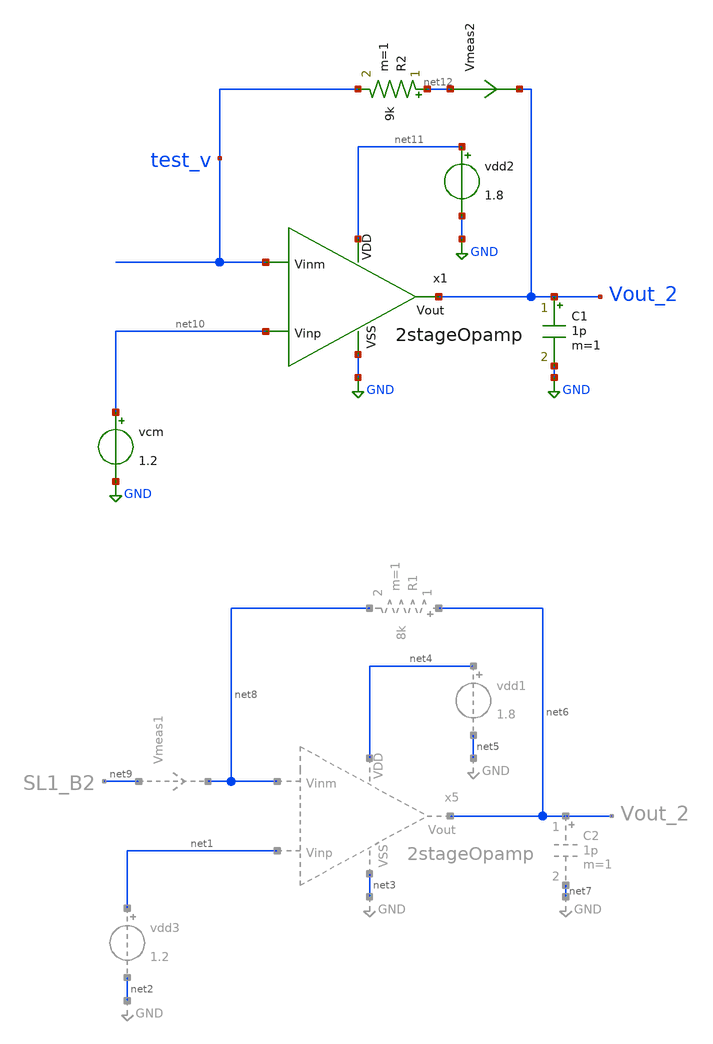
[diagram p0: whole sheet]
** sch_path: xschem/test/xschem/untitled-1.sch
**.subckt untitled-1
x1 net11 test_v net10 Vout_2 GND 2stageOpamp
vdd2 net11 GND 1.8
C1 Vout_2 GND 1p m=1
R2 net12 test_v 9k m=1
Vmeas2 net12 Vout_2 0
.save i(vmeas2)
vcm net10 GND 1.2
**.ends

* expanding   symbol:  amplifiers/dec24/2stageOpamp.sym # of pins=5
** sym_path: amplifiers/dec24/2stageOpamp.sym
** sch_path: amplifiers/dec24/2stageOpamp.sch
.subckt 2stageOpamp VDD Vinm Vinp Vout VSS
*.ipin Vinm
*.ipin Vinp
*.opin Vout
*.ipin VSS
*.ipin VDD
XM8 Vout net1 VSS VSS sky130_fd_pr__nfet_01v8 L=1 W=6 nf=1 ad='int((nf+1)/2) * W/nf * 0.29' as='int((nf+2)/2) * W/nf * 0.29'
+ pd='2*int((nf+1)/2) * (W/nf + 0.29)' ps='2*int((nf+2)/2) * (W/nf + 0.29)' nrd='0.29 / W' nrs='0.29 / W'
+ sa=0 sb=0 sd=0 mult=8 m=8
XM2 Vout Vb1 VDD VDD sky130_fd_pr__pfet_01v8_lvt L=1 W=9 nf=1 ad='int((nf+1)/2) * W/nf * 0.29' as='int((nf+2)/2) * W/nf * 0.29'
+ pd='2*int((nf+1)/2) * (W/nf + 0.29)' ps='2*int((nf+2)/2) * (W/nf + 0.29)' nrd='0.29 / W' nrs='0.29 / W'
+ sa=0 sb=0 sd=0 mult=3 m=3
XM5 net5 Vb3 net6 VSS sky130_fd_pr__nfet_01v8 L=1 W=4 nf=1 ad='int((nf+1)/2) * W/nf * 0.29' as='int((nf+2)/2) * W/nf * 0.29'
+ pd='2*int((nf+1)/2) * (W/nf + 0.29)' ps='2*int((nf+2)/2) * (W/nf + 0.29)' nrd='0.29 / W' nrs='0.29 / W'
+ sa=0 sb=0 sd=0 mult=3 m=3
XM17 net1 Vb3 net7 VSS sky130_fd_pr__nfet_01v8 L=1 W=4 nf=1 ad='int((nf+1)/2) * W/nf * 0.29' as='int((nf+2)/2) * W/nf * 0.29'
+ pd='2*int((nf+1)/2) * (W/nf + 0.29)' ps='2*int((nf+2)/2) * (W/nf + 0.29)' nrd='0.29 / W' nrs='0.29 / W'
+ sa=0 sb=0 sd=0 mult=3 m=3
XM3 net6 net5 VSS VSS sky130_fd_pr__nfet_01v8 L=1 W=8 nf=1 ad='int((nf+1)/2) * W/nf * 0.29' as='int((nf+2)/2) * W/nf * 0.29'
+ pd='2*int((nf+1)/2) * (W/nf + 0.29)' ps='2*int((nf+2)/2) * (W/nf + 0.29)' nrd='0.29 / W' nrs='0.29 / W'
+ sa=0 sb=0 sd=0 mult=1 m=1
XM19 net7 net5 VSS VSS sky130_fd_pr__nfet_01v8 L=1 W=8 nf=1 ad='int((nf+1)/2) * W/nf * 0.29' as='int((nf+2)/2) * W/nf * 0.29'
+ pd='2*int((nf+1)/2) * (W/nf + 0.29)' ps='2*int((nf+2)/2) * (W/nf + 0.29)' nrd='0.29 / W' nrs='0.29 / W'
+ sa=0 sb=0 sd=0 mult=1 m=1
V1 Vb1 GND 1.1
V2 Vb2 GND 0.7
V3 Vb3 GND 0.9
XM11 net8 Vb1 VDD VDD sky130_fd_pr__pfet_01v8_lvt L=1 W=9 nf=1 ad='int((nf+1)/2) * W/nf * 0.29' as='int((nf+2)/2) * W/nf * 0.29'
+ pd='2*int((nf+1)/2) * (W/nf + 0.29)' ps='2*int((nf+2)/2) * (W/nf + 0.29)' nrd='0.29 / W' nrs='0.29 / W'
+ sa=0 sb=0 sd=0 mult=2 m=2
XM1 net6 Vinm net8 VDD sky130_fd_pr__pfet_01v8_lvt L=1 W=8 nf=1 ad='int((nf+1)/2) * W/nf * 0.29' as='int((nf+2)/2) * W/nf * 0.29'
+ pd='2*int((nf+1)/2) * (W/nf + 0.29)' ps='2*int((nf+2)/2) * (W/nf + 0.29)' nrd='0.29 / W' nrs='0.29 / W'
+ sa=0 sb=0 sd=0 mult=3 m=3
XM15 net7 Vinp net8 VDD sky130_fd_pr__pfet_01v8_lvt L=1 W=8 nf=1 ad='int((nf+1)/2) * W/nf * 0.29' as='int((nf+2)/2) * W/nf * 0.29'
+ pd='2*int((nf+1)/2) * (W/nf + 0.29)' ps='2*int((nf+2)/2) * (W/nf + 0.29)' nrd='0.29 / W' nrs='0.29 / W'
+ sa=0 sb=0 sd=0 mult=3 m=3
XM7 net3 Vb1 VDD VDD sky130_fd_pr__pfet_01v8_lvt L=1 W=9 nf=1 ad='int((nf+1)/2) * W/nf * 0.29' as='int((nf+2)/2) * W/nf * 0.29'
+ pd='2*int((nf+1)/2) * (W/nf + 0.29)' ps='2*int((nf+2)/2) * (W/nf + 0.29)' nrd='0.29 / W' nrs='0.29 / W'
+ sa=0 sb=0 sd=0 mult=1 m=1
XM21 net4 Vb1 VDD VDD sky130_fd_pr__pfet_01v8_lvt L=1 W=9 nf=1 ad='int((nf+1)/2) * W/nf * 0.29' as='int((nf+2)/2) * W/nf * 0.29'
+ pd='2*int((nf+1)/2) * (W/nf + 0.29)' ps='2*int((nf+2)/2) * (W/nf + 0.29)' nrd='0.29 / W' nrs='0.29 / W'
+ sa=0 sb=0 sd=0 mult=1 m=1
XM9 net5 Vb2 net3 VDD sky130_fd_pr__pfet_01v8_lvt L=1 W=9 nf=1 ad='int((nf+1)/2) * W/nf * 0.29' as='int((nf+2)/2) * W/nf * 0.29'
+ pd='2*int((nf+1)/2) * (W/nf + 0.29)' ps='2*int((nf+2)/2) * (W/nf + 0.29)' nrd='0.29 / W' nrs='0.29 / W'
+ sa=0 sb=0 sd=0 mult=1 m=1
XM23 net1 Vb2 net4 VDD sky130_fd_pr__pfet_01v8_lvt L=1 W=9 nf=1 ad='int((nf+1)/2) * W/nf * 0.29' as='int((nf+2)/2) * W/nf * 0.29'
+ pd='2*int((nf+1)/2) * (W/nf + 0.29)' ps='2*int((nf+2)/2) * (W/nf + 0.29)' nrd='0.29 / W' nrs='0.29 / W'
+ sa=0 sb=0 sd=0 mult=1 m=1
XC4 net2 Vout sky130_fd_pr__cap_mim_m3_2 W=7 L=7 MF=4 m=4
R4 net1 net2 7k m=1
.ends

.GLOBAL GND
.end
